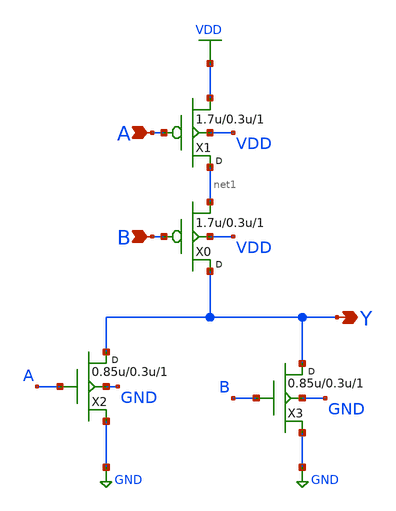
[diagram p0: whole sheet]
** sch_path: lib/xschem/gf180mcu_osu_sc_12T_nor2_1.sch
**.subckt gf180mcu_osu_sc_12T_nor2_1 A B Y
*.ipin A
*.ipin B
*.opin Y
X1 net1 A VDD VDD pmos_3p3 w=1.7u l=0.3u m=1
X0 Y B net1 VDD pmos_3p3 w=1.7u l=0.3u m=1
X2 Y A GND GND nmos_3p3 w=0.85u l=0.3u m=1
X3 Y B GND GND nmos_3p3 w=0.85u l=0.3u m=1
**** begin user architecture code


.inc "/import/yukari1/lrburle/OSU_180/char/techfiles/design.hspice"
.lib "/import/yukari1/lrburle/OSU_180/char/techfiles/sm141064.hspice" typical


**** end user architecture code
**.ends
.GLOBAL VDD
.GLOBAL GND
.end
